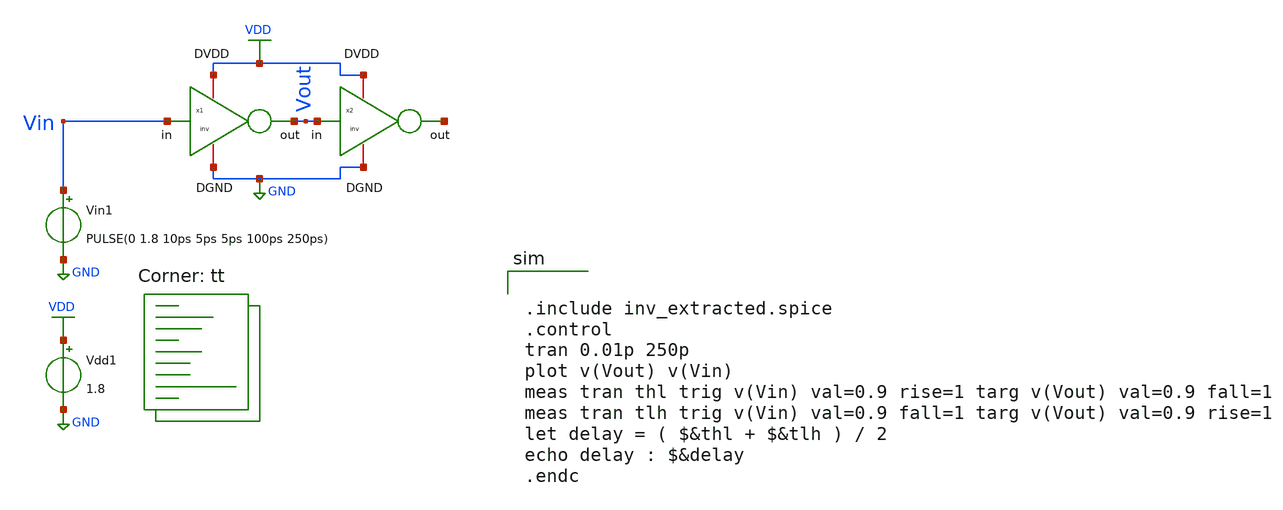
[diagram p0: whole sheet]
** sch_path: tutorial_6/6_1a/tutorial_6_1.sch
**.subckt tutorial_6_1
Vin1 Vin GND PULSE(0 1.8 10ps 5ps 5ps 100ps 250ps)
Vdd1 VDD GND 1.8
x1 VDD Vin Vout GND inv
x2 VDD Vout net1 GND inv
**** begin user architecture code
.lib $::SKYWATER_MODELS/sky130.lib.spice tt


.include inv_extracted.spice
.control
tran 0.01p 250p
plot v(Vout) v(Vin)
meas tran thl trig v(Vin) val=0.9 rise=1 targ v(Vout) val=0.9 fall=1
meas tran tlh trig v(Vin) val=0.9 fall=1 targ v(Vout) val=0.9 rise=1
let delay = ( $&thl + $&tlh ) / 2
echo delay : $&delay
.endc

**** end user architecture code
**.ends
.GLOBAL VDD
.GLOBAL GND
.end
